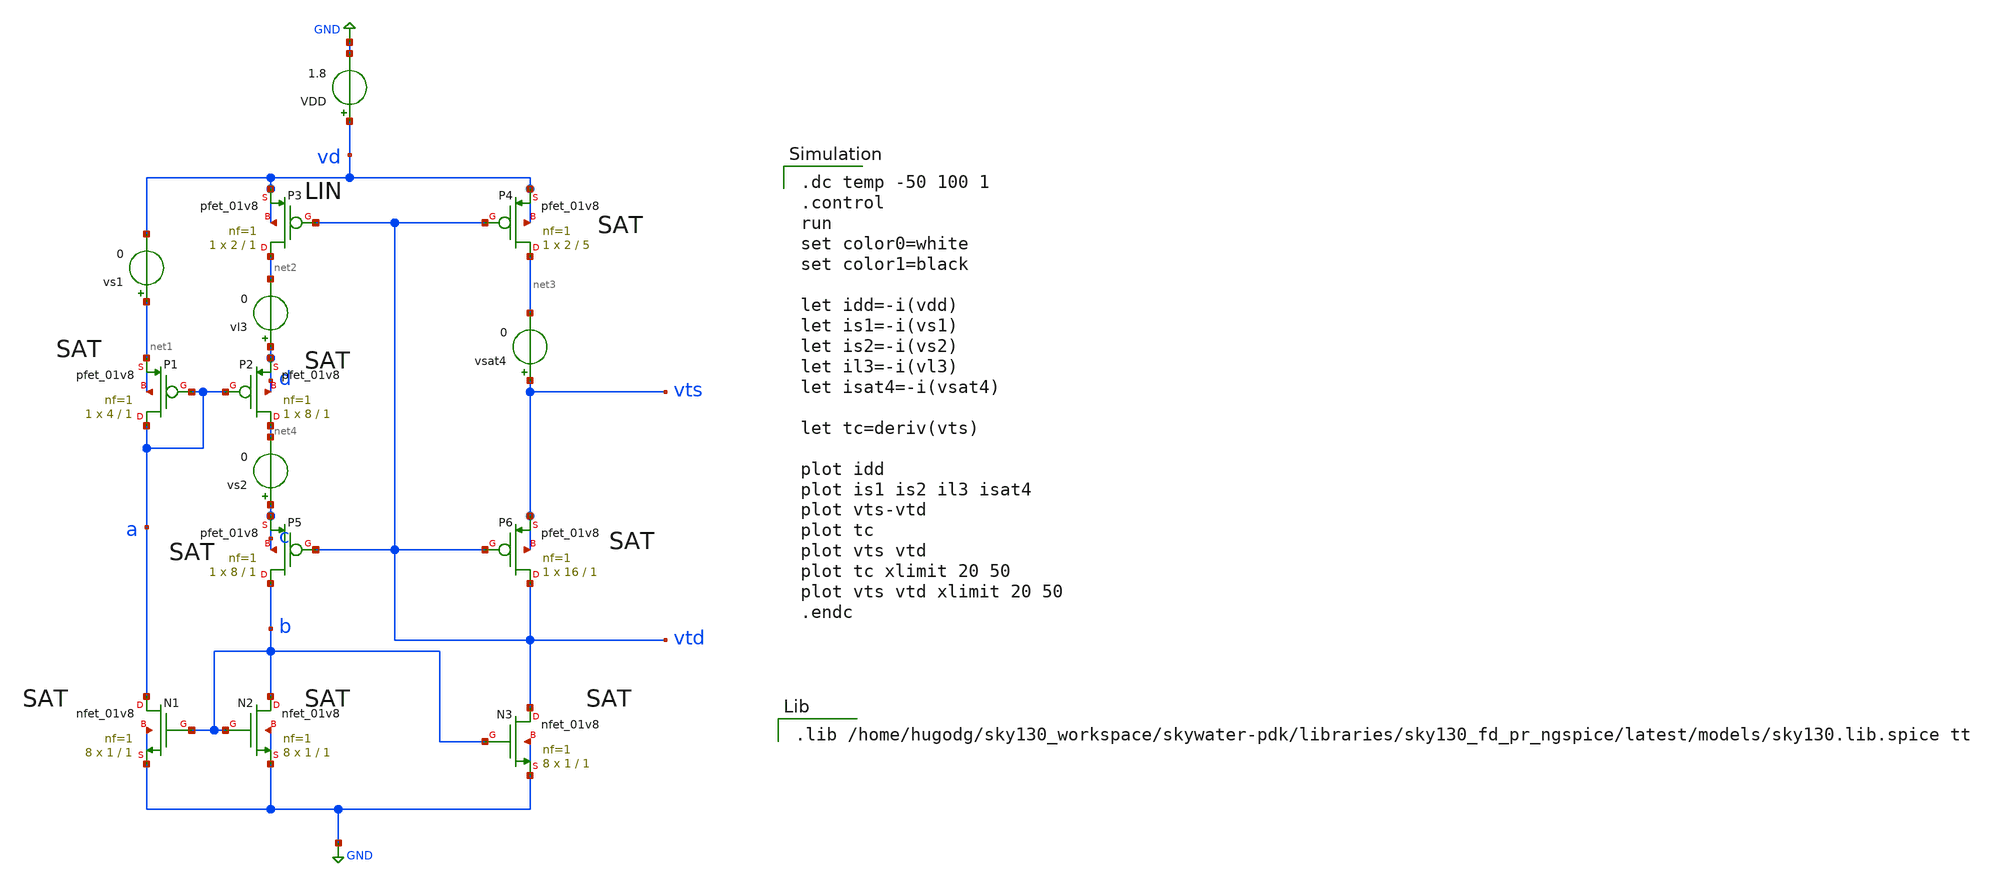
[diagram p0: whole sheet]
** sch_path: sensor/xschem/temp-tb-full.sch
**.subckt temp-tb-full
VDD vd GND 1.8
vs1 net1 vd 0
vs2 c net4 0
vl3 d net2 0
vsat4 vts net3 0
XP1 a a net1 net1 sky130_fd_pr__pfet_01v8 L=1 W=4 nf=1 ad='int((nf+1)/2) * W/nf * 0.29' as='int((nf+2)/2) * W/nf * 0.29'
+ pd='2*int((nf+1)/2) * (W/nf + 0.29)' ps='2*int((nf+2)/2) * (W/nf + 0.29)' nrd='0.29 / W' nrs='0.29 / W'
+ sa=0 sb=0 sd=0 mult=1 m=1
XP2 net4 a d d sky130_fd_pr__pfet_01v8 L=1 W=8 nf=1 ad='int((nf+1)/2) * W/nf * 0.29' as='int((nf+2)/2) * W/nf * 0.29'
+ pd='2*int((nf+1)/2) * (W/nf + 0.29)' ps='2*int((nf+2)/2) * (W/nf + 0.29)' nrd='0.29 / W' nrs='0.29 / W'
+ sa=0 sb=0 sd=0 mult=1 m=1
XP3 net2 vtd vd vd sky130_fd_pr__pfet_01v8 L=1 W=2 nf=1 ad='int((nf+1)/2) * W/nf * 0.29' as='int((nf+2)/2) * W/nf * 0.29'
+ pd='2*int((nf+1)/2) * (W/nf + 0.29)' ps='2*int((nf+2)/2) * (W/nf + 0.29)' nrd='0.29 / W' nrs='0.29 / W'
+ sa=0 sb=0 sd=0 mult=1 m=1
XP4 net3 vtd vd vd sky130_fd_pr__pfet_01v8 L=5 W=2 nf=1 ad='int((nf+1)/2) * W/nf * 0.29' as='int((nf+2)/2) * W/nf * 0.29'
+ pd='2*int((nf+1)/2) * (W/nf + 0.29)' ps='2*int((nf+2)/2) * (W/nf + 0.29)' nrd='0.29 / W' nrs='0.29 / W'
+ sa=0 sb=0 sd=0 mult=1 m=1
XP5 b vtd c c sky130_fd_pr__pfet_01v8 L=1 W=8 nf=1 ad='int((nf+1)/2) * W/nf * 0.29' as='int((nf+2)/2) * W/nf * 0.29'
+ pd='2*int((nf+1)/2) * (W/nf + 0.29)' ps='2*int((nf+2)/2) * (W/nf + 0.29)' nrd='0.29 / W' nrs='0.29 / W'
+ sa=0 sb=0 sd=0 mult=1 m=1
XP6 vtd vtd vts vts sky130_fd_pr__pfet_01v8 L=1 W=16 nf=1 ad='int((nf+1)/2) * W/nf * 0.29' as='int((nf+2)/2) * W/nf * 0.29'
+ pd='2*int((nf+1)/2) * (W/nf + 0.29)' ps='2*int((nf+2)/2) * (W/nf + 0.29)' nrd='0.29 / W' nrs='0.29 / W'
+ sa=0 sb=0 sd=0 mult=1 m=1
XN1 a b GND GND sky130_fd_pr__nfet_01v8 L=1 W=1 nf=1 ad='int((nf+1)/2) * W/nf * 0.29' as='int((nf+2)/2) * W/nf * 0.29'
+ pd='2*int((nf+1)/2) * (W/nf + 0.29)' ps='2*int((nf+2)/2) * (W/nf + 0.29)' nrd='0.29 / W' nrs='0.29 / W'
+ sa=0 sb=0 sd=0 mult=8 m=8
XN2 b b GND GND sky130_fd_pr__nfet_01v8 L=1 W=1 nf=1 ad='int((nf+1)/2) * W/nf * 0.29' as='int((nf+2)/2) * W/nf * 0.29'
+ pd='2*int((nf+1)/2) * (W/nf + 0.29)' ps='2*int((nf+2)/2) * (W/nf + 0.29)' nrd='0.29 / W' nrs='0.29 / W'
+ sa=0 sb=0 sd=0 mult=8 m=8
XN3 vtd b GND GND sky130_fd_pr__nfet_01v8 L=1 W=1 nf=1 ad='int((nf+1)/2) * W/nf * 0.29' as='int((nf+2)/2) * W/nf * 0.29'
+ pd='2*int((nf+1)/2) * (W/nf + 0.29)' ps='2*int((nf+2)/2) * (W/nf + 0.29)' nrd='0.29 / W' nrs='0.29 / W'
+ sa=0 sb=0 sd=0 mult=8 m=8
**** begin user architecture code

.dc temp -50 100 1
.control
run
set color0=white
set color1=black

let idd=-i(vdd)
let is1=-i(vs1)
let is2=-i(vs2)
let il3=-i(vl3)
let isat4=-i(vsat4)

let tc=deriv(vts)

plot idd
plot is1 is2 il3 isat4
plot vts-vtd
plot tc
plot vts vtd
plot tc xlimit 20 50
plot vts vtd xlimit 20 50
.endc



.lib /home/hugodg/sky130_workspace/skywater-pdk/libraries/sky130_fd_pr_ngspice/latest/models/sky130.lib.spice tt

**** end user architecture code
**.ends
.GLOBAL GND
.end
